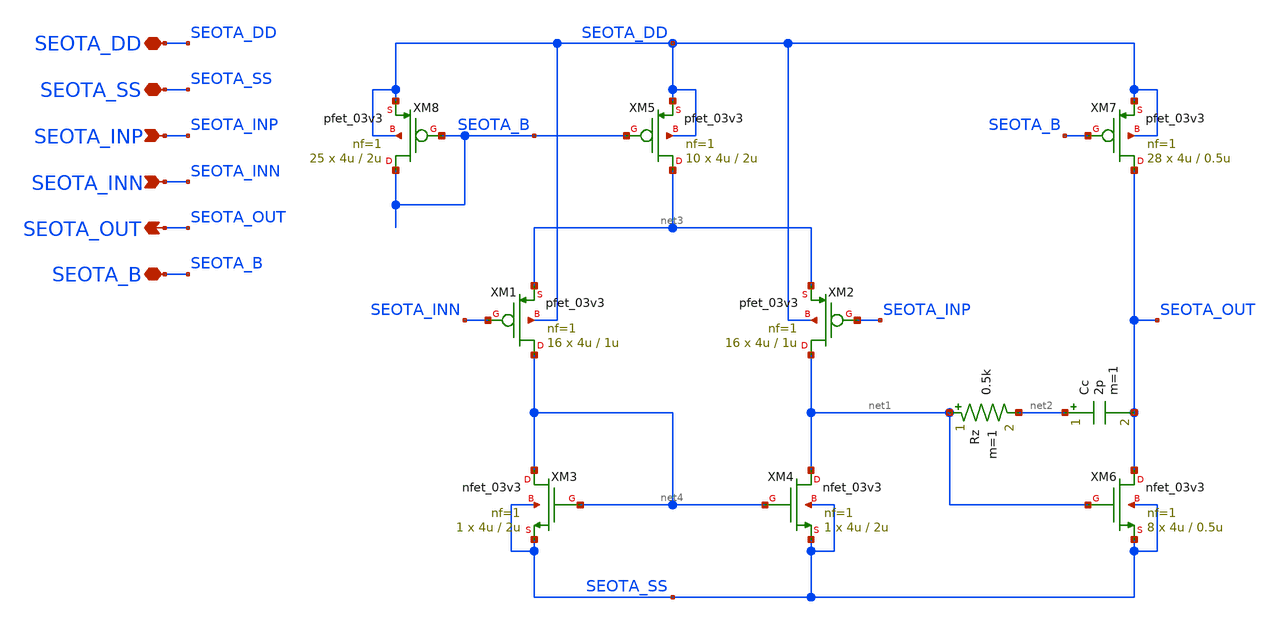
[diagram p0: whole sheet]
** sch_path: Design_Files/IC Design/Schematic/SE_OTA/SE_OTA.sch
**.subckt SE_OTA SEOTA_DD SEOTA_SS SEOTA_INP SEOTA_INN SEOTA_OUT SEOTA_B
*.iopin SEOTA_DD
*.iopin SEOTA_SS
*.ipin SEOTA_INP
*.ipin SEOTA_INN
*.opin SEOTA_OUT
*.iopin SEOTA_B
XM4 net1 net4 SEOTA_SS SEOTA_SS nfet_03v3 L=2u W=4u nf=1 ad='int((nf+1)/2) * W/nf * 0.18u' as='int((nf+2)/2) * W/nf * 0.18u'
+ pd='2*int((nf+1)/2) * (W/nf + 0.18u)' ps='2*int((nf+2)/2) * (W/nf + 0.18u)' nrd='0.18u / W' nrs='0.18u / W'
+ sa=0 sb=0 sd=0 m=1
XM3 net4 net4 SEOTA_SS SEOTA_SS nfet_03v3 L=2u W=4u nf=1 ad='int((nf+1)/2) * W/nf * 0.18u' as='int((nf+2)/2) * W/nf * 0.18u'
+ pd='2*int((nf+1)/2) * (W/nf + 0.18u)' ps='2*int((nf+2)/2) * (W/nf + 0.18u)' nrd='0.18u / W' nrs='0.18u / W'
+ sa=0 sb=0 sd=0 m=1
XM1 net4 SEOTA_INN net3 SEOTA_DD pfet_03v3 L=1u W=4u nf=1 ad='int((nf+1)/2) * W/nf * 0.18u' as='int((nf+2)/2) * W/nf * 0.18u'
+ pd='2*int((nf+1)/2) * (W/nf + 0.18u)' ps='2*int((nf+2)/2) * (W/nf + 0.18u)' nrd='0.18u / W' nrs='0.18u / W'
+ sa=0 sb=0 sd=0 m=16
XM2 net1 SEOTA_INP net3 SEOTA_DD pfet_03v3 L=1u W=4u nf=1 ad='int((nf+1)/2) * W/nf * 0.18u' as='int((nf+2)/2) * W/nf * 0.18u'
+ pd='2*int((nf+1)/2) * (W/nf + 0.18u)' ps='2*int((nf+2)/2) * (W/nf + 0.18u)' nrd='0.18u / W' nrs='0.18u / W'
+ sa=0 sb=0 sd=0 m=16
XM7 SEOTA_OUT SEOTA_B SEOTA_DD SEOTA_DD pfet_03v3 L=0.5u W=4u nf=1 ad='int((nf+1)/2) * W/nf * 0.18u'
+ as='int((nf+2)/2) * W/nf * 0.18u' pd='2*int((nf+1)/2) * (W/nf + 0.18u)' ps='2*int((nf+2)/2) * (W/nf + 0.18u)'
+ nrd='0.18u / W' nrs='0.18u / W' sa=0 sb=0 sd=0 m=28
Rz net1 net2 0.5k m=1
XM5 net3 SEOTA_B SEOTA_DD SEOTA_DD pfet_03v3 L=2u W=4u nf=1 ad='int((nf+1)/2) * W/nf * 0.18u' as='int((nf+2)/2) * W/nf * 0.18u'
+ pd='2*int((nf+1)/2) * (W/nf + 0.18u)' ps='2*int((nf+2)/2) * (W/nf + 0.18u)' nrd='0.18u / W' nrs='0.18u / W'
+ sa=0 sb=0 sd=0 m=10
XM6 SEOTA_OUT net1 SEOTA_SS SEOTA_SS nfet_03v3 L=0.5u W=4u nf=1 ad='int((nf+1)/2) * W/nf * 0.18u' as='int((nf+2)/2) * W/nf * 0.18u'
+ pd='2*int((nf+1)/2) * (W/nf + 0.18u)' ps='2*int((nf+2)/2) * (W/nf + 0.18u)' nrd='0.18u / W' nrs='0.18u / W'
+ sa=0 sb=0 sd=0 m=8
XM8 SEOTA_B SEOTA_B SEOTA_DD SEOTA_DD pfet_03v3 L=2u W=4u nf=1 ad='int((nf+1)/2) * W/nf * 0.18u' as='int((nf+2)/2) * W/nf * 0.18u'
+ pd='2*int((nf+1)/2) * (W/nf + 0.18u)' ps='2*int((nf+2)/2) * (W/nf + 0.18u)' nrd='0.18u / W' nrs='0.18u / W'
+ sa=0 sb=0 sd=0 m=25
Cc net2 SEOTA_OUT 2p m=1
**.ends
.end
